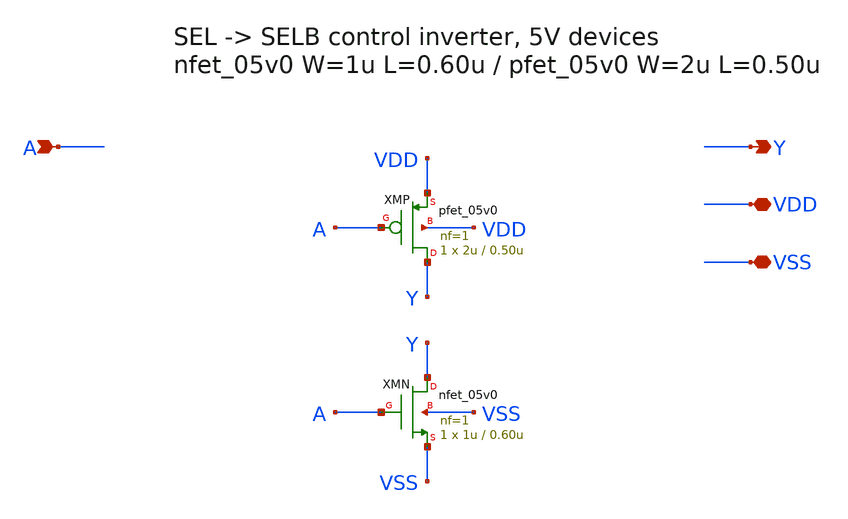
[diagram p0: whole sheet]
** sch_path: inverter_matrix/inv_ctrl_5v0.sch
**.subckt inv_ctrl_5v0 A Y VDD VSS
*.ipin A
*.opin Y
*.iopin VDD
*.iopin VSS
XMP Y A VDD VDD pfet_05v0 L=0.50u W=2u nf=1 ad='int((nf+1)/2) * W/nf * 0.18u' as='int((nf+2)/2) * W/nf * 0.18u'
+ pd='2*int((nf+1)/2) * (W/nf + 0.18u)' ps='2*int((nf+2)/2) * (W/nf + 0.18u)' nrd='0.18u / W' nrs='0.18u / W'
+ sa=0 sb=0 sd=0 m=1
XMN Y A VSS VSS nfet_05v0 L=0.60u W=1u nf=1 ad='int((nf+1)/2) * W/nf * 0.18u' as='int((nf+2)/2) * W/nf * 0.18u'
+ pd='2*int((nf+1)/2) * (W/nf + 0.18u)' ps='2*int((nf+2)/2) * (W/nf + 0.18u)' nrd='0.18u / W' nrs='0.18u / W'
+ sa=0 sb=0 sd=0 m=1
**.ends
.end
